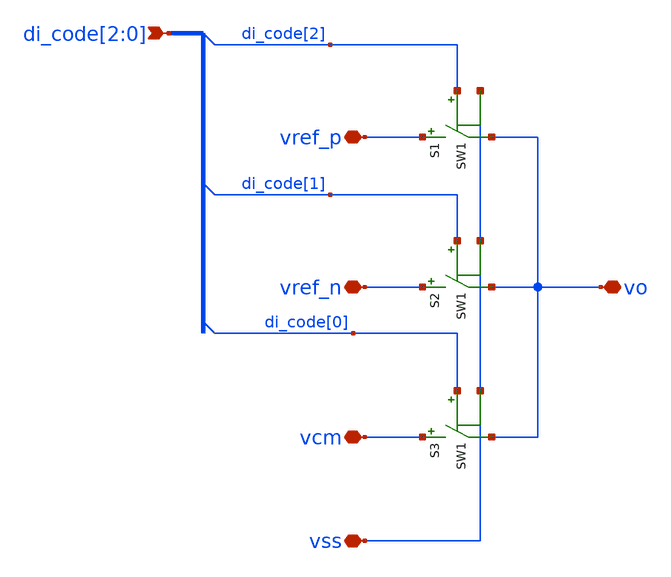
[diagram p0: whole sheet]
** sch_path: xschem/sw_dac.sch
**.subckt sw_dac di_code[2],di_code[1],di_code[0] vref_p vref_n vo vss vcm
*.ipin di_code[2],di_code[1],di_code[0]
*.iopin vref_p
*.iopin vref_n
*.iopin vo
*.iopin vss
*.iopin vcm
S1 vref_p vo di_code[2] vss SW1
S2 vref_n vo di_code[1] vss SW1
S3 vcm vo di_code[0] vss SW1
**.ends
**** begin user architecture code
.MODEL SW1 SW( VT=0.75 VH=0.01 RON=ron ROFF=roff )
**** end user architecture code
.end
